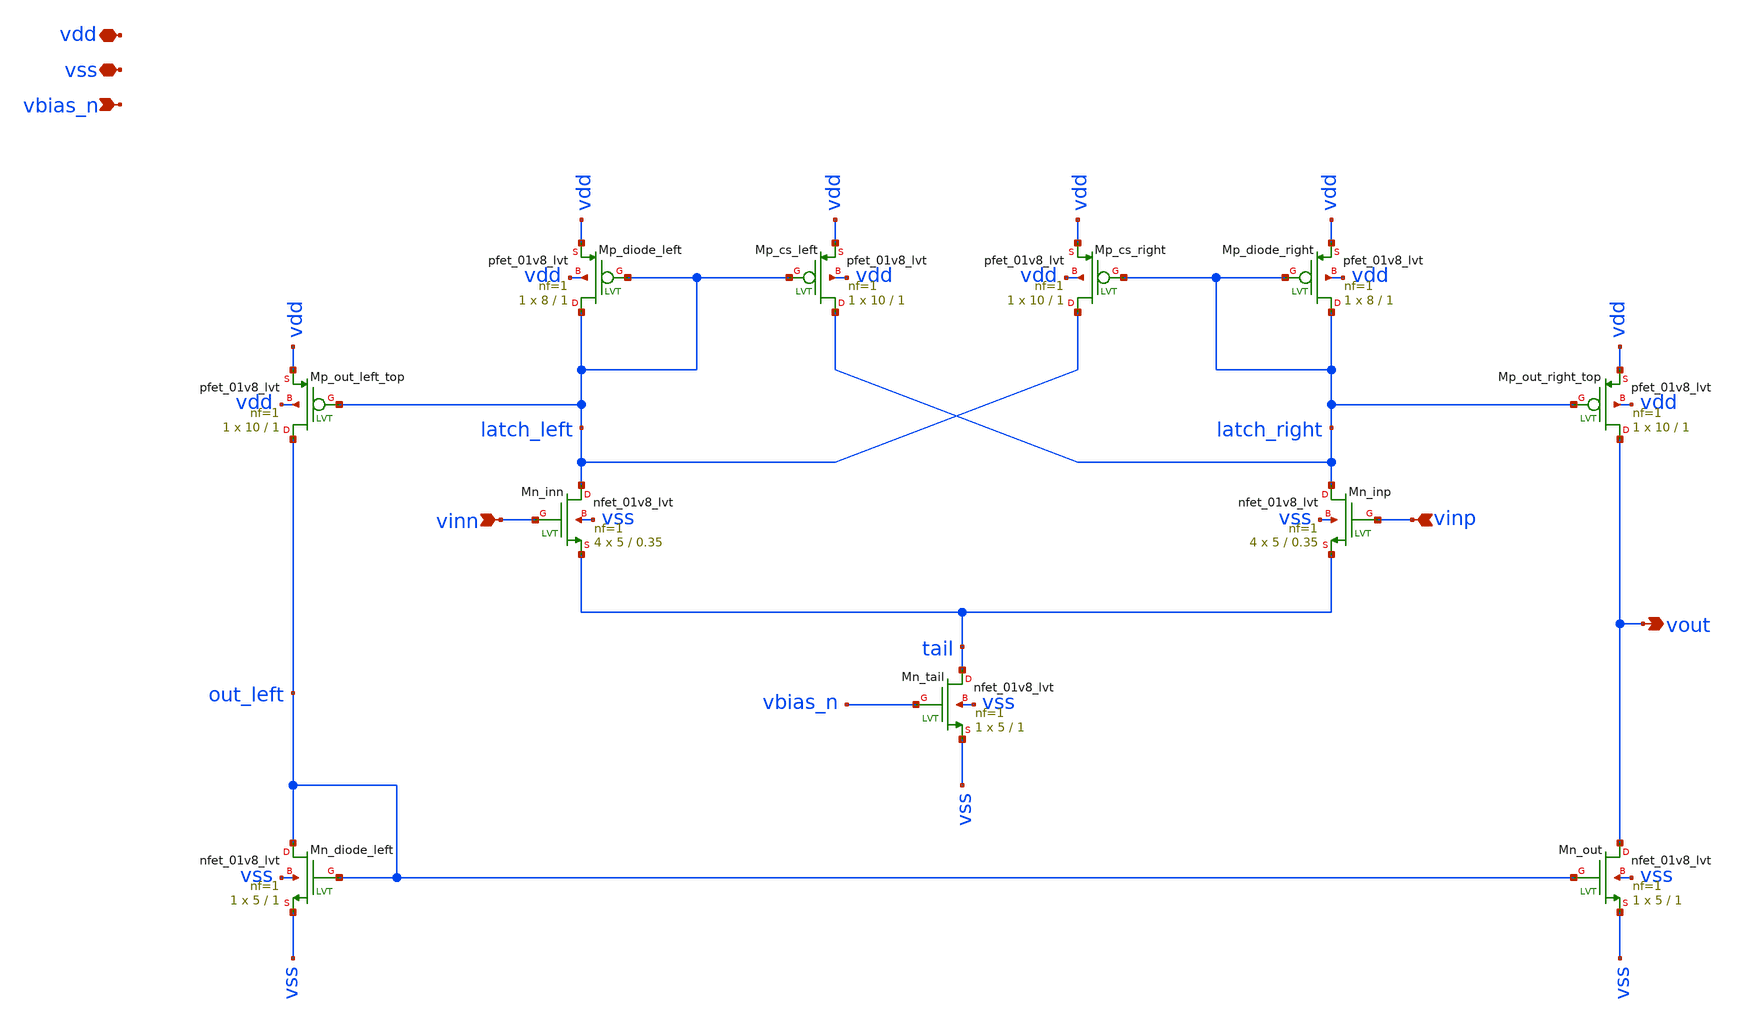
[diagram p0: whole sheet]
** sch_path: xsch/ip/comparators/comp_n/comp_n.sch
**.subckt comp_n vdd vout vss vbias_n vinn vinp
*.iopin vdd
*.opin vout
*.iopin vss
*.ipin vbias_n
*.ipin vinn
*.ipin vinp
XMn_diode_left out_left out_left vss vss sky130_fd_pr__nfet_01v8_lvt L=1 W=5 nf=1 ad='int((nf+1)/2) * W/nf * 0.29'
+ as='int((nf+2)/2) * W/nf * 0.29' pd='2*int((nf+1)/2) * (W/nf + 0.29)' ps='2*int((nf+2)/2) * (W/nf + 0.29)'
+ nrd='0.29 / W' nrs='0.29 / W' sa=0 sb=0 sd=0 mult=1 m=1
XMp_out_left_top out_left latch_left vdd vdd sky130_fd_pr__pfet_01v8_lvt L=1 W=10 nf=1 ad='int((nf+1)/2) * W/nf * 0.29'
+ as='int((nf+2)/2) * W/nf * 0.29' pd='2*int((nf+1)/2) * (W/nf + 0.29)' ps='2*int((nf+2)/2) * (W/nf + 0.29)'
+ nrd='0.29 / W' nrs='0.29 / W' sa=0 sb=0 sd=0 mult=1 m=1
XMn_out vout out_left vss vss sky130_fd_pr__nfet_01v8_lvt L=1 W=5 nf=1 ad='int((nf+1)/2) * W/nf * 0.29'
+ as='int((nf+2)/2) * W/nf * 0.29' pd='2*int((nf+1)/2) * (W/nf + 0.29)' ps='2*int((nf+2)/2) * (W/nf + 0.29)'
+ nrd='0.29 / W' nrs='0.29 / W' sa=0 sb=0 sd=0 mult=1 m=1
XMn_tail tail vbias_n vss vss sky130_fd_pr__nfet_01v8_lvt L=1 W=5 nf=1 ad='int((nf+1)/2) * W/nf * 0.29'
+ as='int((nf+2)/2) * W/nf * 0.29' pd='2*int((nf+1)/2) * (W/nf + 0.29)' ps='2*int((nf+2)/2) * (W/nf + 0.29)'
+ nrd='0.29 / W' nrs='0.29 / W' sa=0 sb=0 sd=0 mult=1 m=1
XMn_inn latch_left vinn tail vss sky130_fd_pr__nfet_01v8_lvt L=0.35 W=5 nf=1 ad='int((nf+1)/2) * W/nf * 0.29'
+ as='int((nf+2)/2) * W/nf * 0.29' pd='2*int((nf+1)/2) * (W/nf + 0.29)' ps='2*int((nf+2)/2) * (W/nf + 0.29)'
+ nrd='0.29 / W' nrs='0.29 / W' sa=0 sb=0 sd=0 mult=4 m=4
XMn_inp latch_right vinp tail vss sky130_fd_pr__nfet_01v8_lvt L=0.35 W=5 nf=1 ad='int((nf+1)/2) * W/nf * 0.29'
+ as='int((nf+2)/2) * W/nf * 0.29' pd='2*int((nf+1)/2) * (W/nf + 0.29)' ps='2*int((nf+2)/2) * (W/nf + 0.29)'
+ nrd='0.29 / W' nrs='0.29 / W' sa=0 sb=0 sd=0 mult=4 m=4
XMp_diode_left latch_left latch_left vdd vdd sky130_fd_pr__pfet_01v8_lvt L=1 W=8 nf=1 ad='int((nf+1)/2) * W/nf * 0.29'
+ as='int((nf+2)/2) * W/nf * 0.29' pd='2*int((nf+1)/2) * (W/nf + 0.29)' ps='2*int((nf+2)/2) * (W/nf + 0.29)'
+ nrd='0.29 / W' nrs='0.29 / W' sa=0 sb=0 sd=0 mult=1 m=1
XMp_cs_left latch_right latch_left vdd vdd sky130_fd_pr__pfet_01v8_lvt L=1 W=10 nf=1 ad='int((nf+1)/2) * W/nf * 0.29'
+ as='int((nf+2)/2) * W/nf * 0.29' pd='2*int((nf+1)/2) * (W/nf + 0.29)' ps='2*int((nf+2)/2) * (W/nf + 0.29)'
+ nrd='0.29 / W' nrs='0.29 / W' sa=0 sb=0 sd=0 mult=1 m=1
XMp_cs_right latch_left latch_right vdd vdd sky130_fd_pr__pfet_01v8_lvt L=1 W=10 nf=1 ad='int((nf+1)/2) * W/nf * 0.29'
+ as='int((nf+2)/2) * W/nf * 0.29' pd='2*int((nf+1)/2) * (W/nf + 0.29)' ps='2*int((nf+2)/2) * (W/nf + 0.29)'
+ nrd='0.29 / W' nrs='0.29 / W' sa=0 sb=0 sd=0 mult=1 m=1
XMp_diode_right latch_right latch_right vdd vdd sky130_fd_pr__pfet_01v8_lvt L=1 W=8 nf=1 ad='int((nf+1)/2) * W/nf * 0.29'
+ as='int((nf+2)/2) * W/nf * 0.29' pd='2*int((nf+1)/2) * (W/nf + 0.29)' ps='2*int((nf+2)/2) * (W/nf + 0.29)'
+ nrd='0.29 / W' nrs='0.29 / W' sa=0 sb=0 sd=0 mult=1 m=1
XMp_out_right_top vout latch_right vdd vdd sky130_fd_pr__pfet_01v8_lvt L=1 W=10 nf=1 ad='int((nf+1)/2) * W/nf * 0.29'
+ as='int((nf+2)/2) * W/nf * 0.29' pd='2*int((nf+1)/2) * (W/nf + 0.29)' ps='2*int((nf+2)/2) * (W/nf + 0.29)'
+ nrd='0.29 / W' nrs='0.29 / W' sa=0 sb=0 sd=0 mult=1 m=1
**.ends
.end
